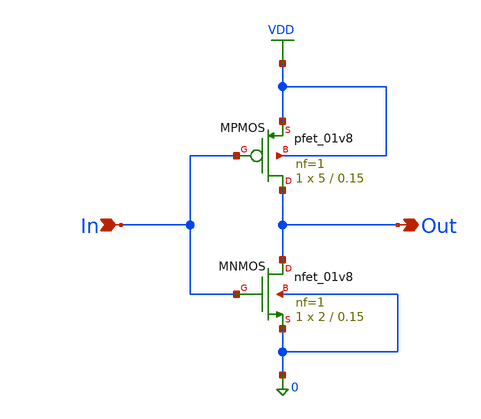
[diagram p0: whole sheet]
** sch_path: cells/full_adder_tg/xschem/inveter_design.sch
**.subckt inveter_design In Out
*.ipin In
*.opin Out
XMNMOS Out In 0 0 sky130_fd_pr__nfet_01v8 L=0.15 W=2 nf=1 ad='int((1 + 1)/2) * 2 / 1 * 0.29' as='int((1 + 2)/2) * 2 / 1 * 0.29'
+ pd='2*int((1 + 1)/2) * (2 / 1 + 0.29)' ps='2*int((1 + 2)/2) * (2 / 1 + 0.29)' nrd='0.29 / 2 ' nrs='0.29 / 2 '
+ sa=0 sb=0 sd=0 mult=1 m=1
XMPMOS Out In VDD VDD sky130_fd_pr__pfet_01v8 L=0.15 W=5 nf=1 ad='int((1 + 1)/2) * 5 / 1 * 0.29' as='int((1 + 2)/2) * 5 / 1 * 0.29'
+ pd='2*int((1 + 1)/2) * (5 / 1 + 0.29)' ps='2*int((1 + 2)/2) * (5 / 1 + 0.29)' nrd='0.29 / 5 ' nrs='0.29 / 5 '
+ sa=0 sb=0 sd=0 mult=1 m=1
**.ends
.GLOBAL VDD
.end
